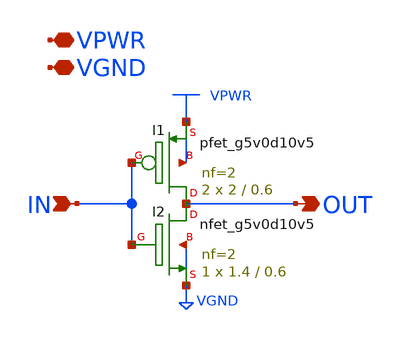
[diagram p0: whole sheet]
** sch_path: common/hvsbt_inv_x2.sch
* Copyright 2023 David Mitchell Bailey
* Licensed under the Apache License, Version 2.0 (the "License");
* you may not use this file except in compliance with the License.
* You may obtain a copy of the License at
* https://www.apache.org/licenses/LICENSE-2.0
* Unless required by applicable law or agreed to in writing, software
* distributed under the License is distributed on an "AS IS" BASIS,
* WITHOUT WARRANTIES OR CONDITIONS OF ANY KIND, either express or implied.
* See the License for the specific language governing permissions and
* limitations under the License.
**.subckt hvsbt_inv_x2 IN OUT VPWR VGND
*.ipin IN
*.opin OUT
*.iopin VPWR
*.iopin VGND
XI2 OUT IN VGND VGND sky130_fd_pr__nfet_g5v0d10v5 L=0.6 W=1.4 nf=2 ad='int((nf+1)/2) * W/nf * 0.29' as='int((nf+2)/2) * W/nf * 0.29'
+ pd='2*int((nf+1)/2) * (W/nf + 0.29)' ps='2*int((nf+2)/2) * (W/nf + 0.29)' nrd='0.29 / W' nrs='0.29 / W'
+ sa=0 sb=0 sd=0 mult=1 m=1
XI1 OUT IN VPWR VPWR sky130_fd_pr__pfet_g5v0d10v5 L=0.6 W=2 nf=2 ad='int((nf+1)/2) * W/nf * 0.29' as='int((nf+2)/2) * W/nf * 0.29'
+ pd='2*int((nf+1)/2) * (W/nf + 0.29)' ps='2*int((nf+2)/2) * (W/nf + 0.29)' nrd='0.29 / W' nrs='0.29 / W'
+ sa=0 sb=0 sd=0 mult=2 m=2
**.ends
.end
